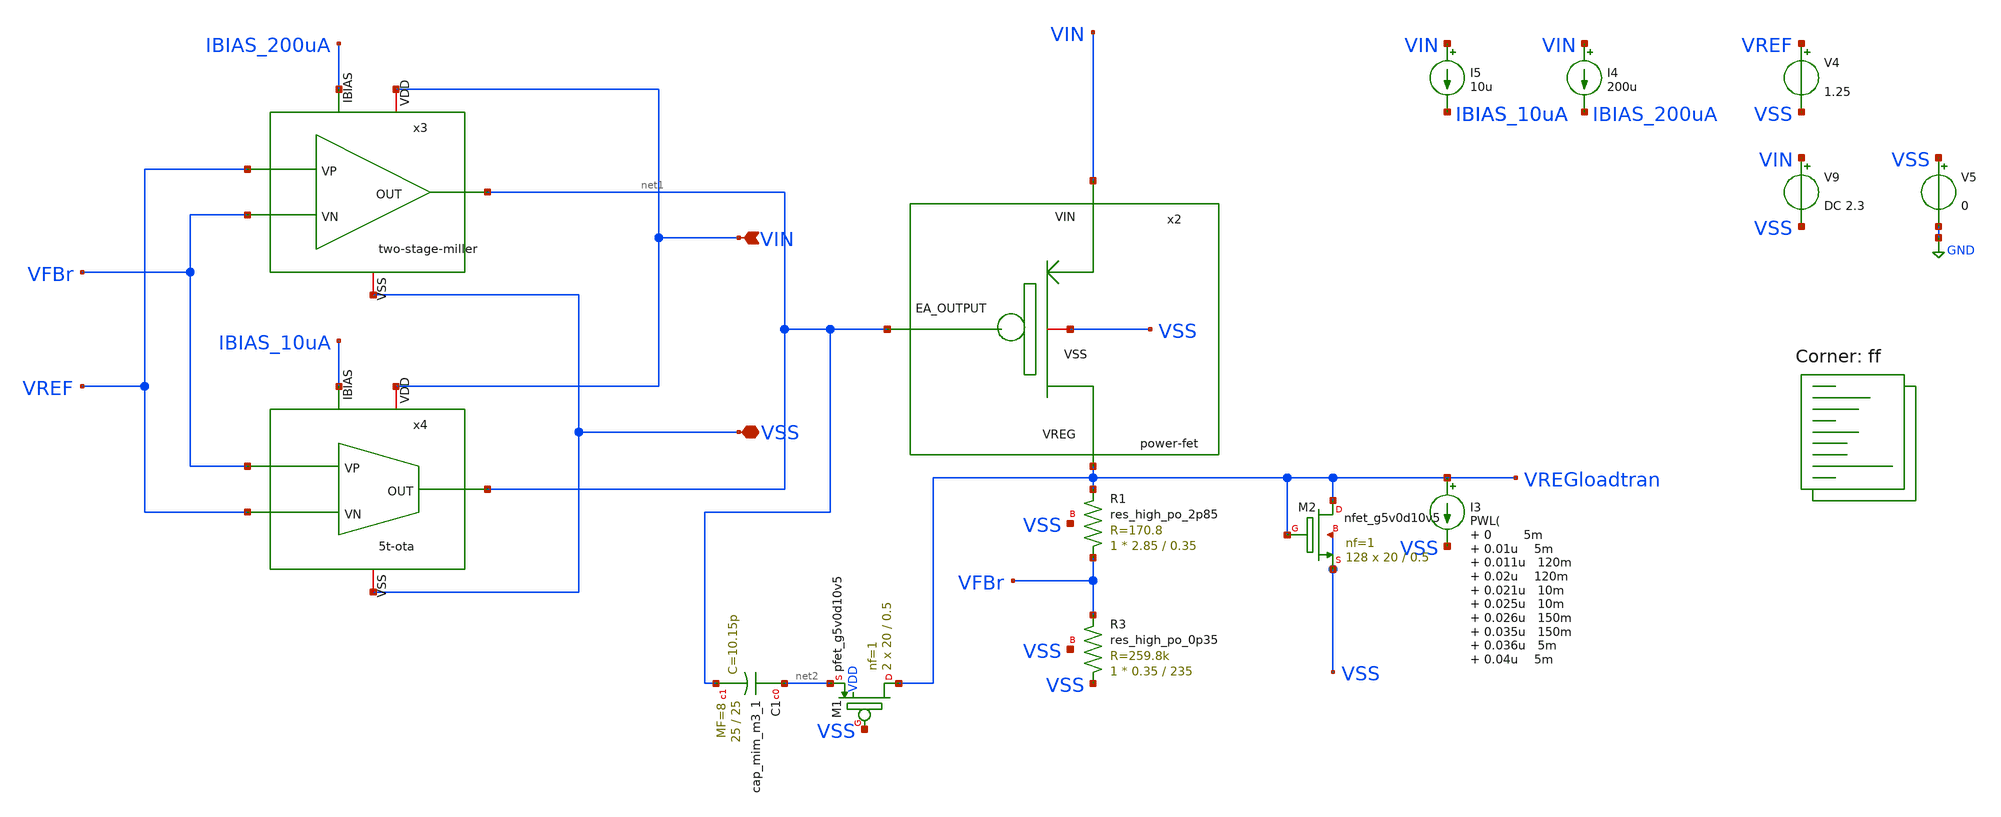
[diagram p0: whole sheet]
** sch_path: bandgap/testbench/untitled-1.sch
**.subckt untitled-1 VIN VSS
*.ipin VIN
*.iopin VSS
x2 VIN VSS net1 VREGloadtran power-fet
XR3 VSS VFBr VSS sky130_fd_pr__res_high_po_0p35 L=235 mult=1 m=1
XR1 VFBr VREGloadtran VSS sky130_fd_pr__res_high_po_2p85 L=0.35 mult=1 m=1
x3 VIN net1 VREF VFBr IBIAS_200uA VSS two-stage-miller
x4 VIN net1 IBIAS_10uA VREF VFBr VSS 5t-ota
I4 VIN IBIAS_200uA 200u
I3 VREGloadtran VSS PWL( 0 5m 0.01u 5m 0.011u 120m 0.02u 120m 0.021u 10m 0.025u 10m 0.026u 150m
+ 0.035u 150m 0.036u 5m 0.04u 5m
)
V4 VREF VSS 1.25
V5 VSS GND 0
V9 VIN VSS DC 2.3
I5 VIN IBIAS_10uA 10u
XM2 VREGloadtran VREGloadtran VSS VSS sky130_fd_pr__nfet_g5v0d10v5 L=0.5 W=20 nf=1 ad='int((nf+1)/2) * W/nf * 0.29'
+ as='int((nf+2)/2) * W/nf * 0.29' pd='2*int((nf+1)/2) * (W/nf + 0.29)' ps='2*int((nf+2)/2) * (W/nf + 0.29)'
+ nrd='0.29 / W' nrs='0.29 / W' sa=0 sb=0 sd=0 mult=128 m=128
XC1 net2 net1 sky130_fd_pr__cap_mim_m3_1 W=25 L=25 MF=8 m=8
XM1 VREGloadtran VSS net2 VDD sky130_fd_pr__pfet_g5v0d10v5 L=0.5 W=20 nf=1 ad='int((nf+1)/2) * W/nf * 0.29'
+ as='int((nf+2)/2) * W/nf * 0.29' pd='2*int((nf+1)/2) * (W/nf + 0.29)' ps='2*int((nf+2)/2) * (W/nf + 0.29)'
+ nrd='0.29 / W' nrs='0.29 / W' sa=0 sb=0 sd=0 mult=2 m=2
**** begin user architecture code



.temp 27
.control

tran 0.01n 0.32u

* Nominal output voltage (from regulation region)
let Vout_nom = 1.25
let Vout_95  = 0.95*Vout_nom

* Find Vin where Vout crosses 95%
meas dc Vin_do find v(vin) when v(vreg)=Vout_95

* Measure Vout at that Vin (for completeness)
meas dc Vout_do find v(vreg) when v(vreg)=Vout_95

* Compute dropout voltage
let Vdo = Vin_do - Vout_do

* Compute overshoot, undershoot and peak-to-peak voltage
meas tran Vout_max MAX v(VREGloadtran)
meas tran Vout_min MIN v(VREGloadtran)
let vpp = Vout_max - Vout_min

print Vin_do Vout_do Vdo
print Vout_max Vout_min Vpp
plot VREGloadtran
plot VREGloadtran2
plot VREG
plot VIN
plot I(Vmeas)

.endc


.lib $::SKYWATER_MODELS/sky130.lib.spice ff
**** end user architecture code
**.ends
.GLOBAL GND
.end
